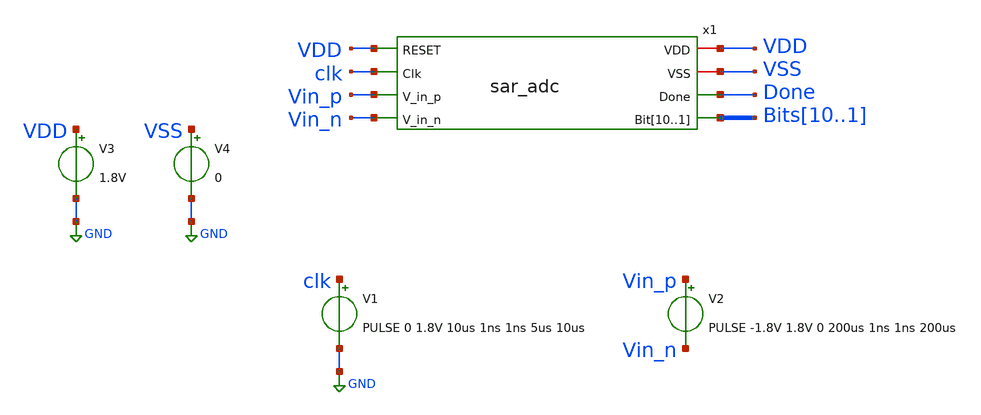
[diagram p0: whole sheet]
** sch_path: xschem/tests/sar_adc/sar_adc_test.sch
**.subckt sar_adc_test
V3 VDD GND 1.8V
V4 VSS GND 0
x1 VDD VSS VDD clk Vin_p Vin_n Done Bits10 Bits9 Bits8 Bits7 Bits6 Bits5 Bits4 Bits3 Bits2 Bits1
+ sar_adc
V1 clk GND PULSE 0 1.8V 10us 1ns 1ns 5us 10us
V2 Vin_p Vin_n PULSE -1.8V 1.8V 0 200us 1ns 1ns 200us
**** begin user architecture code
 .lib $::SKYWATER_MODELS/sky130.lib.spice tt
.include $::SKYWATER_STDCELLS/sky130_fd_sc_hd.spice


.options acct list
.temp 25
*vvcc VDD 0 dc 1.8
*vvss VSS 0 0
.control
tran 0.1u 200u
*plot RST_PLS clk+2 Pulse+4
plot Vin_p-Vin_n-2 bits1 bits2+2 bits3+4 bits4+6 bits5+8 bits6+10 bits7+12 bits8+14 bits9+16
+ bits10+18
write sar_adc_test.raw
.endc


**** end user architecture code
**.ends
.GLOBAL GND
.end
